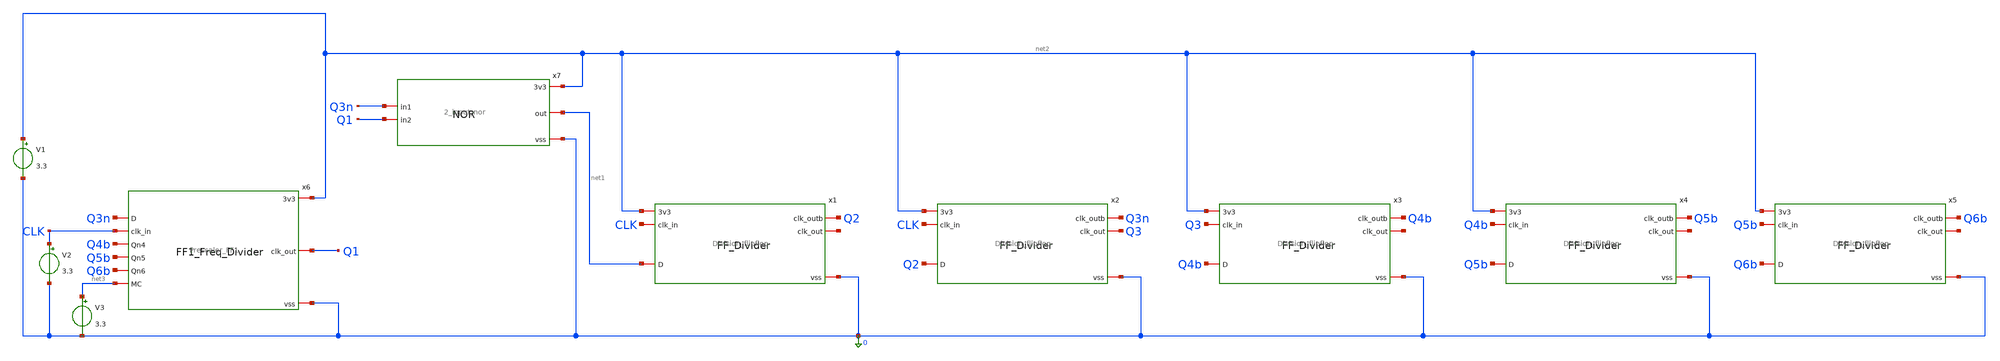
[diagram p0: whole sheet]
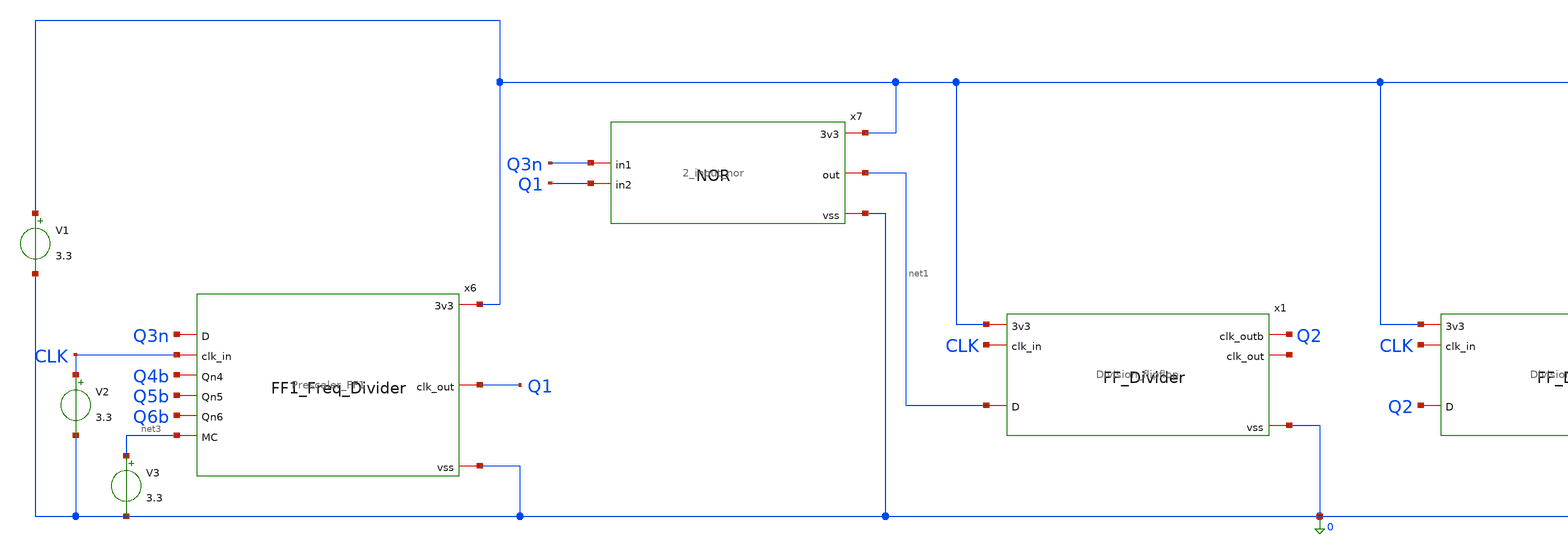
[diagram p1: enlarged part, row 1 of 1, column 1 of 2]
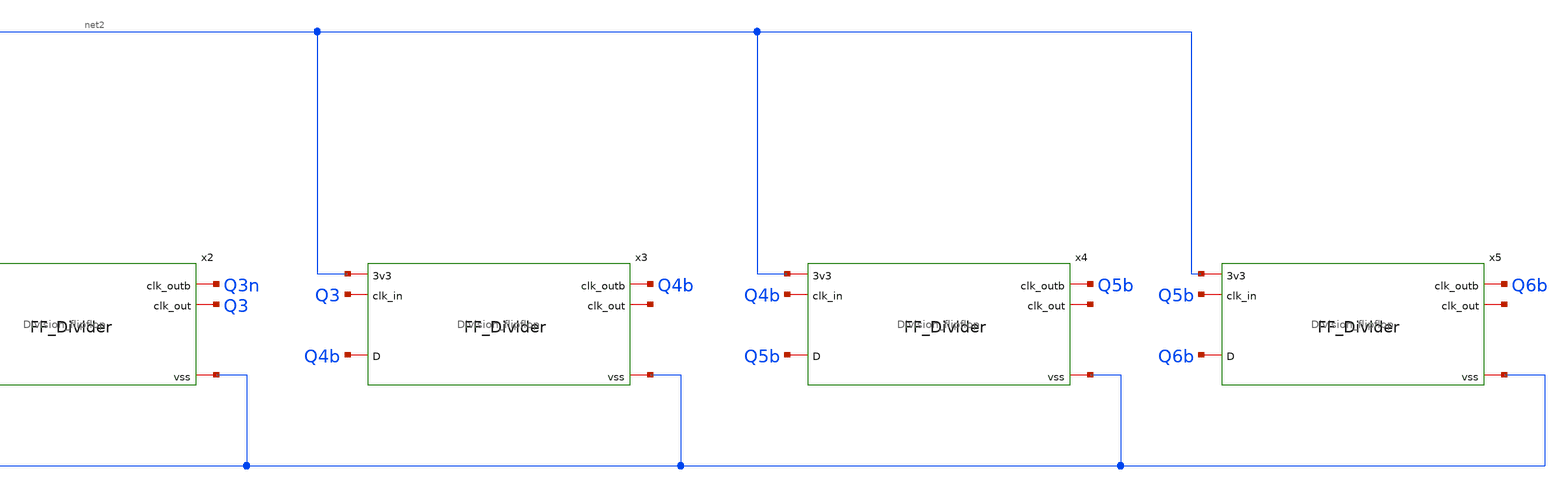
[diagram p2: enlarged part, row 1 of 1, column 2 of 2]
** sch_path: PLL/analog/schematics/32_33_Prescaler.sch
**.subckt 32_33_Prescaler
x6 net2 Q1 Q3n CLK Q4b Q5b Q6b net3 0 Prescaler_FF1
x1 net2 CLK Q2 net4 net1 0 Division_flipflop
x2 net2 CLK Q3n Q3 Q2 0 Division_flipflop
x3 net2 Q3 Q4b net5 Q4b 0 Division_flipflop
x4 net2 Q4b Q5b net6 Q5b 0 Division_flipflop
x5 net2 Q5b Q6b net7 Q6b 0 Division_flipflop
V1 net2 0 3.3
V2 CLK 0 3.3
V3 net3 0 3.3
x7 net2 Q3n Q1 net1 0 2_input_nor
**** begin user architecture code



.include /foss/pdks/gf180mcuD/libs.tech/ngspice/design.ngspice
.lib /foss/pdks/gf180mcuD/libs.tech/ngspice/sm141064.ngspice typical
* Output load: adjust to the next stage's input capacitance.
C_TEST_OUT Q6b 0 10f
.ic V(Q1)=0 V(Q2)=0 V(Q3)=0
.ic V(Q4b)=3.3 V(Q5b)=3.3 V(Q6b)=3.3
.control
set noaskquit
set num_threads=1
set numdgt=8
set wr_singlescale
set wr_vecnames

* Input frequency in Hz.
let fclk = 600e6
let period = 1/fclk
let pulsewidth = period/2 - 1p
let stop_time = 1000*period
let settle_time = 300*period
let zoom_end = settle_time + 12*period

foreach mc 0 3.3
  reset
  option reltol=1e-4 abstol=1e-12 vntol=1e-6

  alter V1 dc = 3.3
  alter V2 dc = 0
  alter @V2[pulse] = [ 0 3.3 1n 1p 1p $&pulsewidth $&period ]
  alter V3 dc = $mc

  save v(CLK) v(Q1) v(Q2) v(Q3) v(Q4b) v(Q5b) v(Q6b) i(V1)

  echo
  echo ===== MC = $mc V =====
  tran 2p $&stop_time 0 2p

  * Measure ten input and ten output periods after settling.
  let span_in = 0
  let span_out = 0
  meas tran span_in TRIG v(CLK) VAL=1.65 RISE=1 TD=$&settle_time TARG v(CLK) VAL=1.65 RISE=11 TD=$&settle_time
  meas tran span_out TRIG v(Q6b) VAL=1.65 RISE=1 TD=$&settle_time TARG v(Q6b) VAL=1.65 RISE=11 TD=$&settle_time

  if span_in > 0
    if span_out > 0
      let input_Hz = 10/span_in
      let output_MHz = (10/span_out)/1e6
      let measured_division = span_out/span_in
      print input_Hz output_MHz measured_division

      * Check ten individual periods for irregular division.
      let edge = 1
      let period_min = 1
      let period_max = 0
      repeat 10
        let next_edge = edge + 1
        meas tran cycle_period TRIG v(Q6b) VAL=1.65 RISE=$&edge TD=$&settle_time TARG v(Q6b) VAL=1.65 RISE=$&next_edge TD=$&settle_time
        if cycle_period < period_min
          let period_min = cycle_period
        end
        if cycle_period > period_max
          let period_max = cycle_period
        end
        let edge = next_edge
      end

      let division_min = period_min*input_Hz
      let division_max = period_max*input_Hz
      print division_min division_max
    else
      echo OUTPUT PERIOD MEASUREMENT FAILED: inspect Q6b and the earlier stages.
    end
  else
    echo INPUT PERIOD MEASUREMENT FAILED: check V2 and the CLK net.
  end

  meas tran output_min MIN v(Q6b) FROM=$&settle_time TO=$&stop_time
  meas tran output_max MAX v(Q6b) FROM=$&settle_time TO=$&stop_time

  meas tran supply_current AVG i(V1) FROM=$&settle_time TO=$&stop_time
  let supply_power_mW = -3.3*supply_current*1000
  print supply_power_mW

  plot v(CLK) v(Q1) v(Q2) v(Q3) xlimit $&settle_time $&zoom_end
  plot v(Q3) v(Q4b) v(Q5b) v(Q6b) xlimit $&settle_time $&stop_time

  wrdata prescaler_MC{$mc}.txt v(CLK) v(Q1) v(Q2) v(Q3) v(Q4b) v(Q5b) v(Q6b) i(V1)
end
.endc



**** end user architecture code
**.ends
.end
